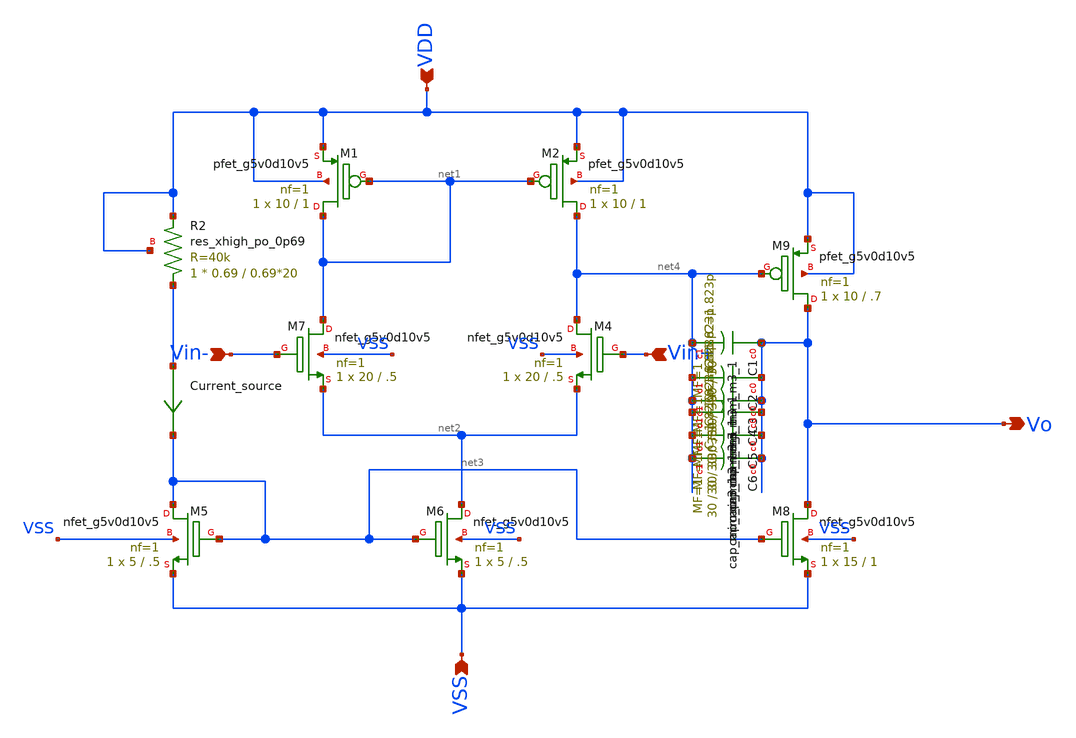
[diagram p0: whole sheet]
** sch_path: hw01/xschem/hw01.sch
**.subckt hw01 VDD Vin- Vin+ VSS Vo
*.ipin VDD
*.ipin Vin-
*.ipin Vin+
*.ipin VSS
*.opin Vo
XM4 net4 Vin+ net2 VSS sky130_fd_pr__nfet_g5v0d10v5 L=.5 W=20 nf=1 ad='int((nf+1)/2) * W/nf * 0.29' as='int((nf+2)/2) * W/nf * 0.29'
+ pd='2*int((nf+1)/2) * (W/nf + 0.29)' ps='2*int((nf+2)/2) * (W/nf + 0.29)' nrd='0.29 / W' nrs='0.29 / W'
+ sa=0 sb=0 sd=0 mult=1 m=1
XM5 net3 net3 VSS VSS sky130_fd_pr__nfet_g5v0d10v5 L=.5 W=5 nf=1 ad='int((nf+1)/2) * W/nf * 0.29' as='int((nf+2)/2) * W/nf * 0.29'
+ pd='2*int((nf+1)/2) * (W/nf + 0.29)' ps='2*int((nf+2)/2) * (W/nf + 0.29)' nrd='0.29 / W' nrs='0.29 / W'
+ sa=0 sb=0 sd=0 mult=1 m=1
XM6 net2 net3 VSS VSS sky130_fd_pr__nfet_g5v0d10v5 L=.5 W=5 nf=1 ad='int((nf+1)/2) * W/nf * 0.29' as='int((nf+2)/2) * W/nf * 0.29'
+ pd='2*int((nf+1)/2) * (W/nf + 0.29)' ps='2*int((nf+2)/2) * (W/nf + 0.29)' nrd='0.29 / W' nrs='0.29 / W'
+ sa=0 sb=0 sd=0 mult=1 m=1
XM8 Vo net3 VSS VSS sky130_fd_pr__nfet_g5v0d10v5 L=1 W=15 nf=1 ad='int((nf+1)/2) * W/nf * 0.29' as='int((nf+2)/2) * W/nf * 0.29'
+ pd='2*int((nf+1)/2) * (W/nf + 0.29)' ps='2*int((nf+2)/2) * (W/nf + 0.29)' nrd='0.29 / W' nrs='0.29 / W'
+ sa=0 sb=0 sd=0 mult=1 m=1
XM7 net1 Vin- net2 VSS sky130_fd_pr__nfet_g5v0d10v5 L=.5 W=20 nf=1 ad='int((nf+1)/2) * W/nf * 0.29' as='int((nf+2)/2) * W/nf * 0.29'
+ pd='2*int((nf+1)/2) * (W/nf + 0.29)' ps='2*int((nf+2)/2) * (W/nf + 0.29)' nrd='0.29 / W' nrs='0.29 / W'
+ sa=0 sb=0 sd=0 mult=1 m=1
Current_source net3 net3 0
.save i(current_source)
XC1 Vo net4 sky130_fd_pr__cap_mim_m3_1 W=30 L=30 MF=1 m=1
XR2 net3 VDD VDD sky130_fd_pr__res_xhigh_po_0p69 L=0.69*20 mult=1 m=1
XM9 Vo net4 VDD VDD sky130_fd_pr__pfet_g5v0d10v5 L=.7 W=10 nf=1 ad='int((nf+1)/2) * W/nf * 0.29' as='int((nf+2)/2) * W/nf * 0.29'
+ pd='2*int((nf+1)/2) * (W/nf + 0.29)' ps='2*int((nf+2)/2) * (W/nf + 0.29)' nrd='0.29 / W' nrs='0.29 / W'
+ sa=0 sb=0 sd=0 mult=1 m=1
XM2 net4 net1 VDD VDD sky130_fd_pr__pfet_g5v0d10v5 L=1 W=10 nf=1 ad='int((nf+1)/2) * W/nf * 0.29' as='int((nf+2)/2) * W/nf * 0.29'
+ pd='2*int((nf+1)/2) * (W/nf + 0.29)' ps='2*int((nf+2)/2) * (W/nf + 0.29)' nrd='0.29 / W' nrs='0.29 / W'
+ sa=0 sb=0 sd=0 mult=1 m=1
XM1 net1 net1 VDD VDD sky130_fd_pr__pfet_g5v0d10v5 L=1 W=10 nf=1 ad='int((nf+1)/2) * W/nf * 0.29' as='int((nf+2)/2) * W/nf * 0.29'
+ pd='2*int((nf+1)/2) * (W/nf + 0.29)' ps='2*int((nf+2)/2) * (W/nf + 0.29)' nrd='0.29 / W' nrs='0.29 / W'
+ sa=0 sb=0 sd=0 mult=1 m=1
XC2 Vo net4 sky130_fd_pr__cap_mim_m3_1 W=30 L=30 MF=1 m=1
XC3 Vo net4 sky130_fd_pr__cap_mim_m3_1 W=30 L=30 MF=1 m=1
XC4 Vo net4 sky130_fd_pr__cap_mim_m3_1 W=30 L=30 MF=1 m=1
XC5 Vo net4 sky130_fd_pr__cap_mim_m3_1 W=30 L=30 MF=1 m=1
XC6 Vo net4 sky130_fd_pr__cap_mim_m3_1 W=30 L=30 MF=1 m=1
**** begin user architecture code

** opencircuitdesign pdks install
.lib $::SKYWATER_MODELS/sky130.lib.spice tt


**** end user architecture code
**.ends
.end
